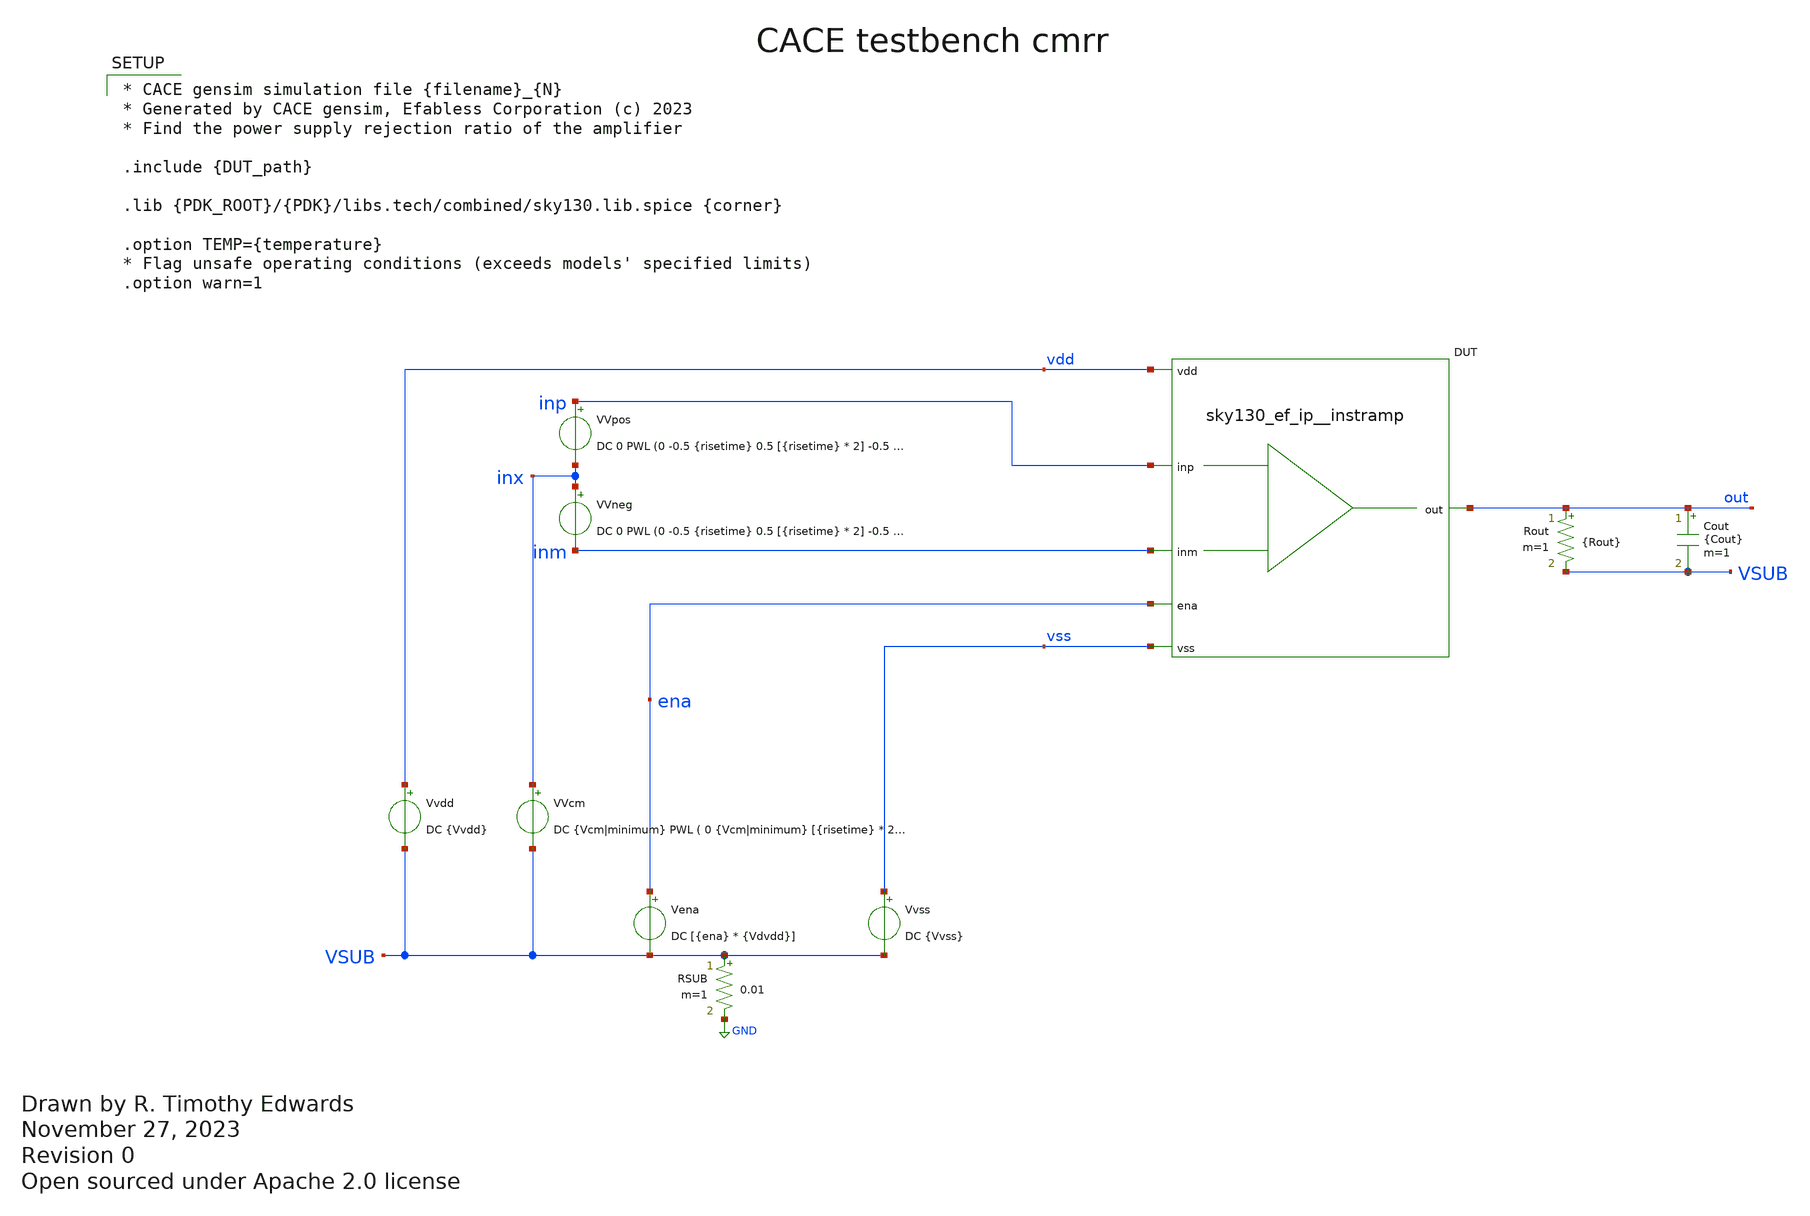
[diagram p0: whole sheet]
** sch_path: cace/cmrr.sch
* Open sourced under Apache 2.0 license
**.subckt cmrr
VVcm inx VSUB DC {Vcm|minimum} PWL ( 0 {Vcm|minimum} [{risetime} * 2] {Vcm|minimum} [{risetime} * 2 +
+ 1e-9] {Vcm|maximum} [{risetime} * 3] {Vcm|maximum} )
Vena ena VSUB DC [{ena} * {Vdvdd}]
Vvss vss VSUB DC {Vvss}
Rout out VSUB {Rout} m=1
Cout out VSUB {Cout} m=1
Vvdd vdd VSUB DC {Vvdd}
RSUB VSUB GND 0.01 m=1
XDUT {PIN|vdd|vdd} {PIN|vss|vss} {PIN|inm|inm} {PIN|inp|inp} {PIN|out|out} {PIN|ena|ena} {DUT_name}
VVpos inp inx DC 0 PWL (0 -0.5 {risetime} 0.5 [{risetime} * 2] -0.5 [{risetime} * 3] 0.5 [{risetime}
+ * 4] -0.5 )
VVneg inx inm DC 0 PWL (0 -0.5 {risetime} 0.5 [{risetime} * 2] -0.5 [{risetime} * 3] 0.5 [{risetime}
+ * 4] -0.5 )
**** begin user architecture code

.control
** CMRR is defined as the change in input offset vs. change in common-mode voltage.
tran [{risetime} * 2 / 100] [{risetime} * 4]
meas tran vhigh1 FIND V(inp) WHEN V(out) = [{Vvdd} / 2] CROSS=1
meas tran vlow1 FIND V(inp) WHEN V(out) = [{Vvdd} / 2] CROSS=2
meas tran vhigh2 FIND V(inp) WHEN V(out) = [{Vvdd} / 2] CROSS=3
meas tran vlow2 FIND V(inp) WHEN V(out) = [{Vvdd} / 2] CROSS=4

let voffset1 = 0.5 * ($&vhigh1 + $&vlow1) - {Vcm|minimum}
let voffset2 = 0.5 * ($&vhigh2 + $&vlow2) - {Vcm|maximum}

let cmrr = ($&voffset1 - $&voffset2) / ({Vcm|maximum} - {Vcm|minimum})
let cmrrdb = 20 * log(abs($&cmrr))

set wr_singlescale
wrdata {simpath}/{filename}_{N}.data $&cmrrdb
quit
.endc



* CACE gensim simulation file {filename}_{N}
* Generated by CACE gensim, Efabless Corporation (c) 2023
* Find the power supply rejection ratio of the amplifier

.include {DUT_path}

.lib {PDK_ROOT}/{PDK}/libs.tech/combined/sky130.lib.spice {corner}

.option TEMP={temperature}
* Flag unsafe operating conditions (exceeds models' specified limits)
.option warn=1


**** end user architecture code
**.ends
.GLOBAL GND
.end
